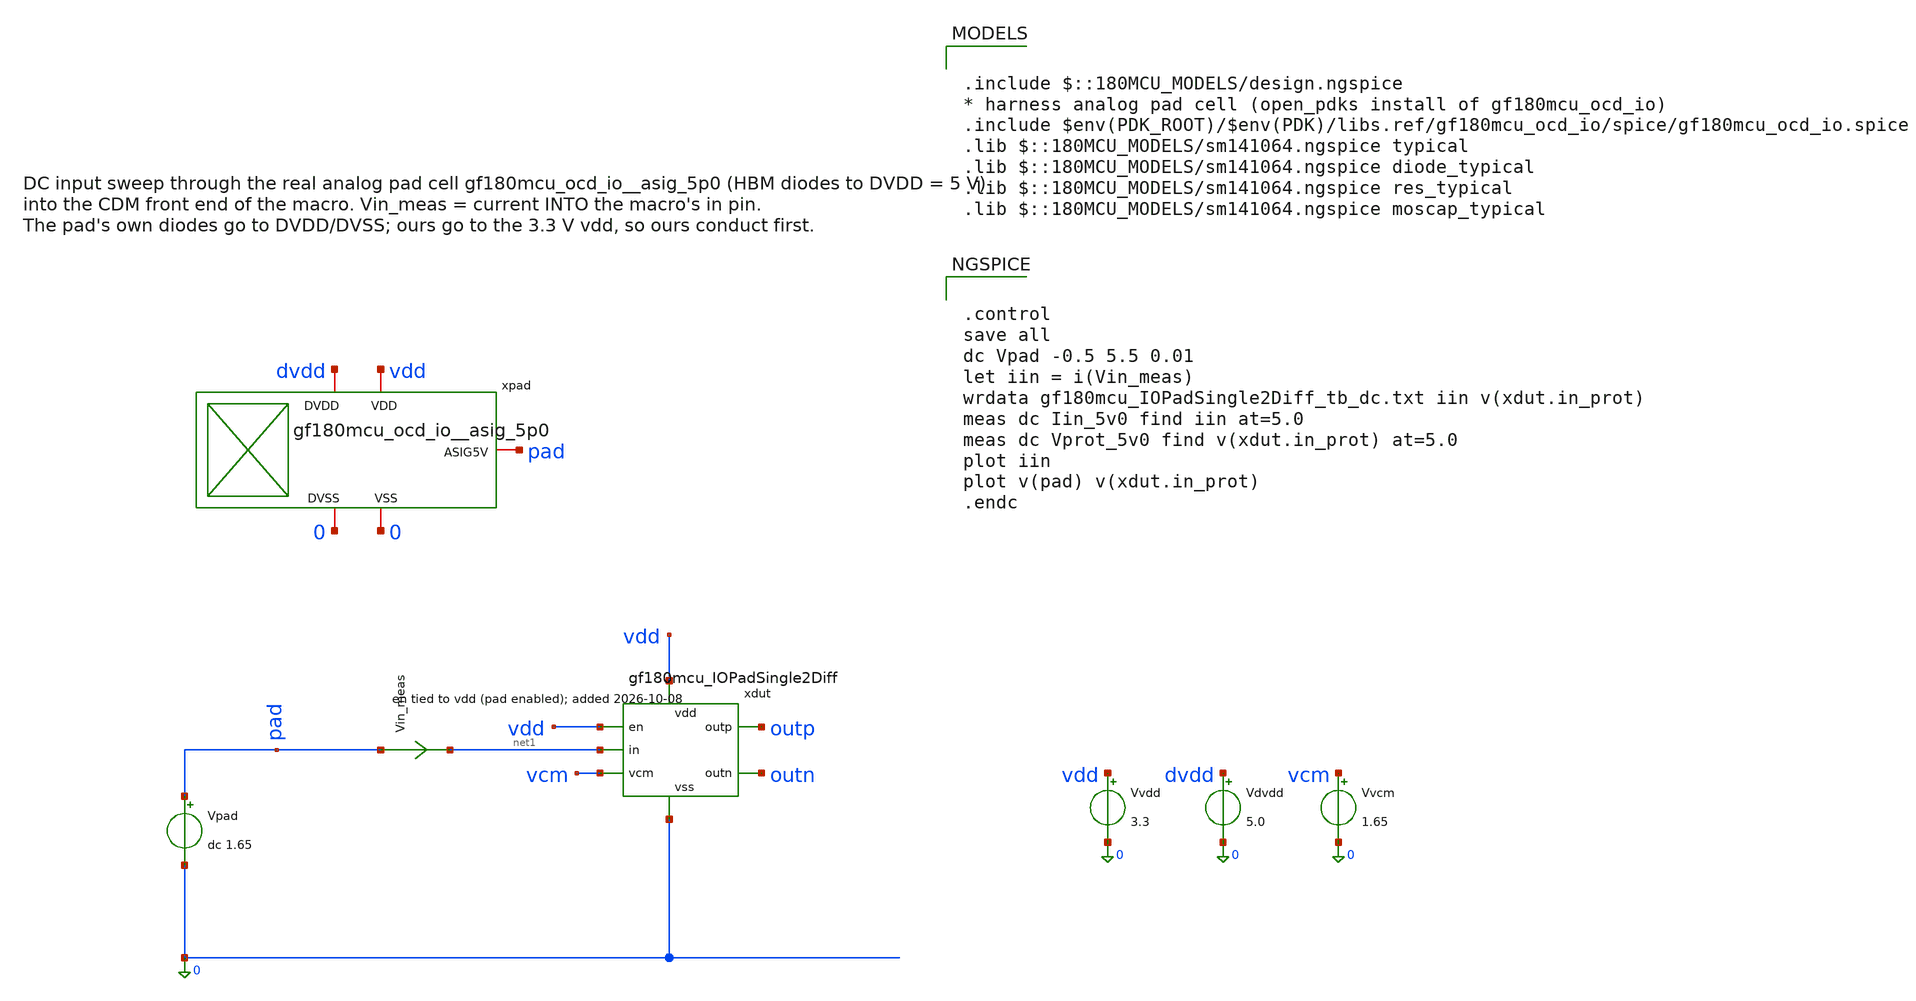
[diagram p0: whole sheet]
** sch_path: macros/gf180mcu_IOPadSingle2Diff/testbenches/xschem/gf180mcu_IOPadSingle2Diff_tb_dc.sch
**.subckt gf180mcu_IOPadSingle2Diff_tb_dc
Vvdd vdd 0 3.3
Vdvdd dvdd 0 5.0
Vvcm vcm 0 1.65
Vpad pad 0 dc 1.65
Vin_meas pad net1 0
.save i(vin_meas)
xdut vdd outp vcm net1 outn 0 vdd gf180mcu_IOPadSingle2Diff
xpad pad dvdd 0 vdd 0 gf180mcu_ocd_io__asig_5p0
**** begin user architecture code


.control
save all
dc Vpad -0.5 5.5 0.01
let iin = i(Vin_meas)
wrdata gf180mcu_IOPadSingle2Diff_tb_dc.txt iin v(xdut.in_prot)
meas dc Iin_5v0 find iin at=5.0
meas dc Vprot_5v0 find v(xdut.in_prot) at=5.0
plot iin
plot v(pad) v(xdut.in_prot)
.endc



.include $::180MCU_MODELS/design.ngspice
* harness analog pad cell (open_pdks install of gf180mcu_ocd_io)
.include $env(PDK_ROOT)/$env(PDK)/libs.ref/gf180mcu_ocd_io/spice/gf180mcu_ocd_io.spice
.lib $::180MCU_MODELS/sm141064.ngspice typical
.lib $::180MCU_MODELS/sm141064.ngspice diode_typical
.lib $::180MCU_MODELS/sm141064.ngspice res_typical
.lib $::180MCU_MODELS/sm141064.ngspice moscap_typical

**** end user architecture code
**.ends

* expanding   symbol:  gf180mcu_IOPadSingle2Diff.sym # of pins=7
** sym_path: macros/gf180mcu_IOPadSingle2Diff/schematic/xschem/gf180mcu_IOPadSingle2Diff.sym
** sch_path: macros/gf180mcu_IOPadSingle2Diff/schematic/xschem/gf180mcu_IOPadSingle2Diff.sch
.subckt gf180mcu_IOPadSingle2Diff vdd outp vcm in outn vss en
*.iopin vdd
*.opin outp
*.ipin vcm
*.ipin in
*.opin outn
*.iopin vss
*.ipin en
XRcdm in_prot in vss ppolyf_u_1k_6p0 r_width=5e-6 r_length=1e-6 m=1
Dcdmp in_prot vdd diode_pd2nw_06v0 area='2u * 12u ' pj='2*2u + 2*12u ' m=1
Dcdmn vss in_prot diode_nd2ps_06v0 area='2u * 12u ' pj='2*2u + 2*12u ' m=1
xinen vdd vss en en_b in_prot in_en vcm InputEnable
xinv vdd vss en en_b EnableInv
.ends


* expanding   symbol:  InputEnable.sym # of pins=7
** sym_path: macros/PadEnable/schematic/xschem/InputEnable.sym
** sch_path: macros/PadEnable/schematic/xschem/InputEnable.sch
.subckt InputEnable vdd vss en en_b pin pout vpark
*.iopin vdd
*.iopin vss
*.ipin en
*.ipin en_b
*.iopin pin
*.iopin pout
*.ipin vpark
XTGP1 pout en_b pin vdd pfet_03v3 L=0.5u W=4u nf=1 ad='int((nf+1)/2) * W/nf * 0.18u' as='int((nf+2)/2) * W/nf * 0.18u'
+ pd='2*int((nf+1)/2) * (W/nf + 0.18u)' ps='2*int((nf+2)/2) * (W/nf + 0.18u)' nrd='0.18u / W' nrs='0.18u / W'
+ sa=0 sb=0 sd=0 m=1
XTGN1 pin en pout vss nfet_03v3 L=0.5u W=4u nf=1 ad='int((nf+1)/2) * W/nf * 0.18u' as='int((nf+2)/2) * W/nf * 0.18u'
+ pd='2*int((nf+1)/2) * (W/nf + 0.18u)' ps='2*int((nf+2)/2) * (W/nf + 0.18u)' nrd='0.18u / W' nrs='0.18u / W'
+ sa=0 sb=0 sd=0 m=1
XTGP2 vpark en pout vdd pfet_03v3 L=0.5u W=4u nf=1 ad='int((nf+1)/2) * W/nf * 0.18u' as='int((nf+2)/2) * W/nf * 0.18u'
+ pd='2*int((nf+1)/2) * (W/nf + 0.18u)' ps='2*int((nf+2)/2) * (W/nf + 0.18u)' nrd='0.18u / W' nrs='0.18u / W'
+ sa=0 sb=0 sd=0 m=1
XTGN2 pout en_b vpark vss nfet_03v3 L=0.5u W=4u nf=1 ad='int((nf+1)/2) * W/nf * 0.18u' as='int((nf+2)/2) * W/nf * 0.18u'
+ pd='2*int((nf+1)/2) * (W/nf + 0.18u)' ps='2*int((nf+2)/2) * (W/nf + 0.18u)' nrd='0.18u / W' nrs='0.18u / W'
+ sa=0 sb=0 sd=0 m=1
.ends


* expanding   symbol:  EnableInv.sym # of pins=4
** sym_path: macros/PadEnable/schematic/xschem/EnableInv.sym
** sch_path: macros/PadEnable/schematic/xschem/EnableInv.sch
.subckt EnableInv vdd vss en en_b
*.iopin vdd
*.iopin vss
*.ipin en
*.opin en_b
XMP en_b en vdd vdd pfet_03v3 L=0.5u W=2u nf=1 ad='int((nf+1)/2) * W/nf * 0.18u' as='int((nf+2)/2) * W/nf * 0.18u'
+ pd='2*int((nf+1)/2) * (W/nf + 0.18u)' ps='2*int((nf+2)/2) * (W/nf + 0.18u)' nrd='0.18u / W' nrs='0.18u / W'
+ sa=0 sb=0 sd=0 m=1
XMN en_b en vss vss nfet_03v3 L=0.5u W=1u nf=1 ad='int((nf+1)/2) * W/nf * 0.18u' as='int((nf+2)/2) * W/nf * 0.18u'
+ pd='2*int((nf+1)/2) * (W/nf + 0.18u)' ps='2*int((nf+2)/2) * (W/nf + 0.18u)' nrd='0.18u / W' nrs='0.18u / W'
+ sa=0 sb=0 sd=0 m=1
.ends

.end
